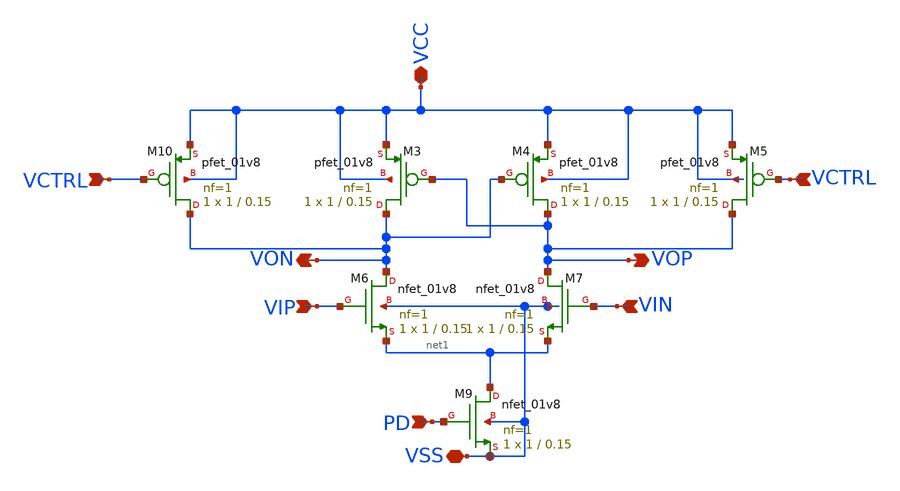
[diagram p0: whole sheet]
** sch_path: xschem/inverterblock.sch
**.subckt inverterblock VIP VON VOP PD VSS VIN VCTRL VCC VCTRL
*.ipin VIP
*.opin VON
*.opin VOP
*.ipin PD
*.iopin VSS
*.ipin VIN
*.ipin VCTRL
*.iopin VCC
*.ipin VCTRL
XM9 net1 PD VSS VSS sky130_fd_pr__nfet_01v8 L=0.15 W=1 nf=1 ad='int((nf+1)/2) * W/nf * 0.29' as='int((nf+2)/2) * W/nf * 0.29'
+ pd='2*int((nf+1)/2) * (W/nf + 0.29)' ps='2*int((nf+2)/2) * (W/nf + 0.29)' nrd='0.29 / W' nrs='0.29 / W'
+ sa=0 sb=0 sd=0 mult=1 m=1
XM10 VON VCTRL VCC VCC sky130_fd_pr__pfet_01v8 L=0.15 W=1 nf=1 ad='int((nf+1)/2) * W/nf * 0.29' as='int((nf+2)/2) * W/nf * 0.29'
+ pd='2*int((nf+1)/2) * (W/nf + 0.29)' ps='2*int((nf+2)/2) * (W/nf + 0.29)' nrd='0.29 / W' nrs='0.29 / W'
+ sa=0 sb=0 sd=0 mult=1 m=1
XM3 VON VOP VCC VCC sky130_fd_pr__pfet_01v8 L=0.15 W=1 nf=1 ad='int((nf+1)/2) * W/nf * 0.29' as='int((nf+2)/2) * W/nf * 0.29'
+ pd='2*int((nf+1)/2) * (W/nf + 0.29)' ps='2*int((nf+2)/2) * (W/nf + 0.29)' nrd='0.29 / W' nrs='0.29 / W'
+ sa=0 sb=0 sd=0 mult=1 m=1
XM4 VOP VON VCC VCC sky130_fd_pr__pfet_01v8 L=0.15 W=1 nf=1 ad='int((nf+1)/2) * W/nf * 0.29' as='int((nf+2)/2) * W/nf * 0.29'
+ pd='2*int((nf+1)/2) * (W/nf + 0.29)' ps='2*int((nf+2)/2) * (W/nf + 0.29)' nrd='0.29 / W' nrs='0.29 / W'
+ sa=0 sb=0 sd=0 mult=1 m=1
XM5 VOP VCTRL VCC VCC sky130_fd_pr__pfet_01v8 L=0.15 W=1 nf=1 ad='int((nf+1)/2) * W/nf * 0.29' as='int((nf+2)/2) * W/nf * 0.29'
+ pd='2*int((nf+1)/2) * (W/nf + 0.29)' ps='2*int((nf+2)/2) * (W/nf + 0.29)' nrd='0.29 / W' nrs='0.29 / W'
+ sa=0 sb=0 sd=0 mult=1 m=1
XM6 VON VIP net1 VSS sky130_fd_pr__nfet_01v8 L=0.15 W=1 nf=1 ad='int((nf+1)/2) * W/nf * 0.29' as='int((nf+2)/2) * W/nf * 0.29'
+ pd='2*int((nf+1)/2) * (W/nf + 0.29)' ps='2*int((nf+2)/2) * (W/nf + 0.29)' nrd='0.29 / W' nrs='0.29 / W'
+ sa=0 sb=0 sd=0 mult=1 m=1
XM7 VOP VIN net1 VSS sky130_fd_pr__nfet_01v8 L=0.15 W=1 nf=1 ad='int((nf+1)/2) * W/nf * 0.29' as='int((nf+2)/2) * W/nf * 0.29'
+ pd='2*int((nf+1)/2) * (W/nf + 0.29)' ps='2*int((nf+2)/2) * (W/nf + 0.29)' nrd='0.29 / W' nrs='0.29 / W'
+ sa=0 sb=0 sd=0 mult=1 m=1
**.ends
.end
